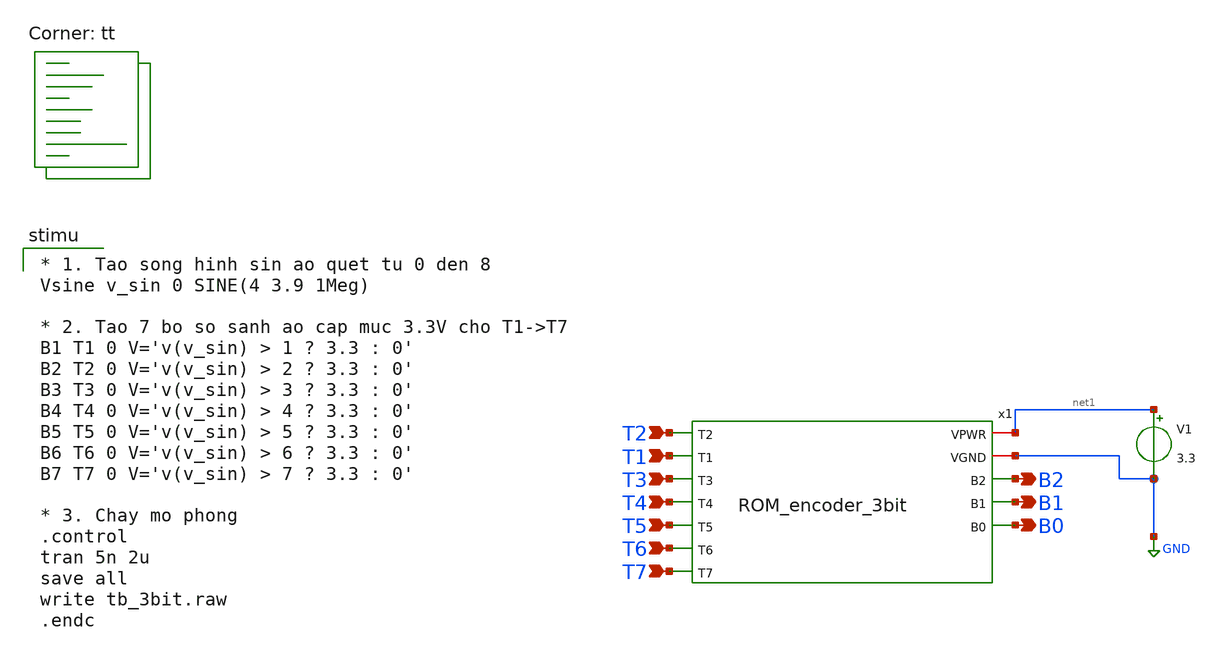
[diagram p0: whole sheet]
** sch_path: tb_rom_encoder_3bit.sch
**.subckt tb_rom_encoder_3bit T1 T2 T3 T4 T5 T6 T7 B2 B1 B0
*.ipin T1
*.ipin T2
*.ipin T3
*.ipin T4
*.ipin T5
*.ipin T6
*.ipin T7
*.opin B2
*.opin B1
*.opin B0
V1 net1 GND 3.3
x1 net1 T2 T1 T3 T4 T5 T6 T7 GND B2 B1 B0 ROM_encoder_3bit
**** begin user architecture code

* 1. Tao song hinh sin ao quet tu 0 den 8
Vsine v_sin 0 SINE(4 3.9 1Meg)

* 2. Tao 7 bo so sanh ao cap muc 3.3V cho T1->T7
B1 T1 0 V='v(v_sin) > 1 ? 3.3 : 0'
B2 T2 0 V='v(v_sin) > 2 ? 3.3 : 0'
B3 T3 0 V='v(v_sin) > 3 ? 3.3 : 0'
B4 T4 0 V='v(v_sin) > 4 ? 3.3 : 0'
B5 T5 0 V='v(v_sin) > 5 ? 3.3 : 0'
B6 T6 0 V='v(v_sin) > 6 ? 3.3 : 0'
B7 T7 0 V='v(v_sin) > 7 ? 3.3 : 0'

* 3. Chay mo phong
.control
tran 5n 2u
save all
write tb_3bit.raw
.endc

.lib $::SKYWATER_MODELS/sky130.lib.spice tt
**** end user architecture code
**.ends

* expanding   symbol:  /home/huydq/ROM_encoder_3bit.sym # of pins=12
** sym_path: ROM_encoder_3bit.sym
** sch_path: ROM_encoder_3bit.sch
.subckt ROM_encoder_3bit VPWR T2 T1 T3 T4 T5 T6 T7 VGND B2 B1 B0
*.ipin T1
*.ipin T2
*.ipin T3
*.ipin T4
*.ipin T5
*.ipin T6
*.ipin T7
*.iopin VGND
*.iopin VPWR
*.opin B0
*.opin B1
*.opin B2
x1 VPWR T2 T1 net4 VGND edge_cell
x2 VPWR T3 T2 net5 VGND edge_cell
x3 VPWR T4 T3 net6 VGND edge_cell
x4 VPWR T5 T4 net7 VGND edge_cell
x5 VPWR T6 T5 net8 VGND edge_cell
x6 VPWR T7 T6 net9 VGND edge_cell
x7 VPWR GND T7 net10 VGND edge_cell
XM7 net1 VGND VPWR VPWR sky130_fd_pr__pfet_g5v0d10v5 L=0.5 W=1 nf=1 ad='int((nf+1)/2) * W/nf * 0.29'
+ as='int((nf+2)/2) * W/nf * 0.29' pd='2*int((nf+1)/2) * (W/nf + 0.29)' ps='2*int((nf+2)/2) * (W/nf + 0.29)'
+ nrd='0.29 / W' nrs='0.29 / W' sa=0 sb=0 sd=0 mult=1 m=1
XM1 net2 VGND VPWR VPWR sky130_fd_pr__pfet_g5v0d10v5 L=0.5 W=1 nf=1 ad='int((nf+1)/2) * W/nf * 0.29'
+ as='int((nf+2)/2) * W/nf * 0.29' pd='2*int((nf+1)/2) * (W/nf + 0.29)' ps='2*int((nf+2)/2) * (W/nf + 0.29)'
+ nrd='0.29 / W' nrs='0.29 / W' sa=0 sb=0 sd=0 mult=1 m=1
XM2 net3 VGND VPWR VPWR sky130_fd_pr__pfet_g5v0d10v5 L=0.5 W=1 nf=1 ad='int((nf+1)/2) * W/nf * 0.29'
+ as='int((nf+2)/2) * W/nf * 0.29' pd='2*int((nf+1)/2) * (W/nf + 0.29)' ps='2*int((nf+2)/2) * (W/nf + 0.29)'
+ nrd='0.29 / W' nrs='0.29 / W' sa=0 sb=0 sd=0 mult=1 m=1
x8 VPWR net1 B0 VGND my_inv_1
x9 VPWR net2 B1 VGND my_inv_1
x10 VPWR net3 B2 VGND my_inv_1
XM3 net1 net4 GND GND sky130_fd_pr__nfet_g5v0d10v5 L=0.5 W=1 nf=1 ad='int((nf+1)/2) * W/nf * 0.29' as='int((nf+2)/2) * W/nf * 0.29'
+ pd='2*int((nf+1)/2) * (W/nf + 0.29)' ps='2*int((nf+2)/2) * (W/nf + 0.29)' nrd='0.29 / W' nrs='0.29 / W'
+ sa=0 sb=0 sd=0 mult=1 m=1
XM4 net2 net5 GND GND sky130_fd_pr__nfet_g5v0d10v5 L=0.5 W=1 nf=1 ad='int((nf+1)/2) * W/nf * 0.29' as='int((nf+2)/2) * W/nf * 0.29'
+ pd='2*int((nf+1)/2) * (W/nf + 0.29)' ps='2*int((nf+2)/2) * (W/nf + 0.29)' nrd='0.29 / W' nrs='0.29 / W'
+ sa=0 sb=0 sd=0 mult=1 m=1
XM5 net1 net6 GND GND sky130_fd_pr__nfet_g5v0d10v5 L=0.5 W=1 nf=1 ad='int((nf+1)/2) * W/nf * 0.29' as='int((nf+2)/2) * W/nf * 0.29'
+ pd='2*int((nf+1)/2) * (W/nf + 0.29)' ps='2*int((nf+2)/2) * (W/nf + 0.29)' nrd='0.29 / W' nrs='0.29 / W'
+ sa=0 sb=0 sd=0 mult=1 m=1
XM6 net2 net6 GND GND sky130_fd_pr__nfet_g5v0d10v5 L=0.5 W=1 nf=1 ad='int((nf+1)/2) * W/nf * 0.29' as='int((nf+2)/2) * W/nf * 0.29'
+ pd='2*int((nf+1)/2) * (W/nf + 0.29)' ps='2*int((nf+2)/2) * (W/nf + 0.29)' nrd='0.29 / W' nrs='0.29 / W'
+ sa=0 sb=0 sd=0 mult=1 m=1
XM8 net3 net7 GND GND sky130_fd_pr__nfet_g5v0d10v5 L=0.5 W=1 nf=1 ad='int((nf+1)/2) * W/nf * 0.29' as='int((nf+2)/2) * W/nf * 0.29'
+ pd='2*int((nf+1)/2) * (W/nf + 0.29)' ps='2*int((nf+2)/2) * (W/nf + 0.29)' nrd='0.29 / W' nrs='0.29 / W'
+ sa=0 sb=0 sd=0 mult=1 m=1
XM9 net1 net8 GND GND sky130_fd_pr__nfet_g5v0d10v5 L=0.5 W=1 nf=1 ad='int((nf+1)/2) * W/nf * 0.29' as='int((nf+2)/2) * W/nf * 0.29'
+ pd='2*int((nf+1)/2) * (W/nf + 0.29)' ps='2*int((nf+2)/2) * (W/nf + 0.29)' nrd='0.29 / W' nrs='0.29 / W'
+ sa=0 sb=0 sd=0 mult=1 m=1
XM10 net3 net8 GND GND sky130_fd_pr__nfet_g5v0d10v5 L=0.5 W=1 nf=1 ad='int((nf+1)/2) * W/nf * 0.29' as='int((nf+2)/2) * W/nf * 0.29'
+ pd='2*int((nf+1)/2) * (W/nf + 0.29)' ps='2*int((nf+2)/2) * (W/nf + 0.29)' nrd='0.29 / W' nrs='0.29 / W'
+ sa=0 sb=0 sd=0 mult=1 m=1
XM11 net2 net9 GND GND sky130_fd_pr__nfet_g5v0d10v5 L=0.5 W=1 nf=1 ad='int((nf+1)/2) * W/nf * 0.29' as='int((nf+2)/2) * W/nf * 0.29'
+ pd='2*int((nf+1)/2) * (W/nf + 0.29)' ps='2*int((nf+2)/2) * (W/nf + 0.29)' nrd='0.29 / W' nrs='0.29 / W'
+ sa=0 sb=0 sd=0 mult=1 m=1
XM12 net3 net9 GND GND sky130_fd_pr__nfet_g5v0d10v5 L=0.5 W=1 nf=1 ad='int((nf+1)/2) * W/nf * 0.29' as='int((nf+2)/2) * W/nf * 0.29'
+ pd='2*int((nf+1)/2) * (W/nf + 0.29)' ps='2*int((nf+2)/2) * (W/nf + 0.29)' nrd='0.29 / W' nrs='0.29 / W'
+ sa=0 sb=0 sd=0 mult=1 m=1
XM13 net1 net10 GND GND sky130_fd_pr__nfet_g5v0d10v5 L=0.5 W=1 nf=1 ad='int((nf+1)/2) * W/nf * 0.29'
+ as='int((nf+2)/2) * W/nf * 0.29' pd='2*int((nf+1)/2) * (W/nf + 0.29)' ps='2*int((nf+2)/2) * (W/nf + 0.29)'
+ nrd='0.29 / W' nrs='0.29 / W' sa=0 sb=0 sd=0 mult=1 m=1
XM14 net2 net10 GND GND sky130_fd_pr__nfet_g5v0d10v5 L=0.5 W=1 nf=1 ad='int((nf+1)/2) * W/nf * 0.29'
+ as='int((nf+2)/2) * W/nf * 0.29' pd='2*int((nf+1)/2) * (W/nf + 0.29)' ps='2*int((nf+2)/2) * (W/nf + 0.29)'
+ nrd='0.29 / W' nrs='0.29 / W' sa=0 sb=0 sd=0 mult=1 m=1
XM15 net3 net10 GND GND sky130_fd_pr__nfet_g5v0d10v5 L=0.5 W=1 nf=1 ad='int((nf+1)/2) * W/nf * 0.29'
+ as='int((nf+2)/2) * W/nf * 0.29' pd='2*int((nf+1)/2) * (W/nf + 0.29)' ps='2*int((nf+2)/2) * (W/nf + 0.29)'
+ nrd='0.29 / W' nrs='0.29 / W' sa=0 sb=0 sd=0 mult=1 m=1
.ends


* expanding   symbol:  /home/huydq/edge_cell.sym # of pins=5
** sym_path: edge_cell.sym
** sch_path: edge_cell.sch
.subckt edge_cell VPWR T_next T_in X_out VGND
*.ipin T_next
*.ipin T_in
*.opin X_out
*.iopin VPWR
*.iopin VGND
x1 VPWR T_next net2 VGND my_inv_1
x2 VPWR net1 X_out VGND my_inv_1
x3 VPWR net1 T_in net2 VGND my_nand_2
.ends


* expanding   symbol:  /home/huydq/my_inv_1.sym # of pins=4
** sym_path: my_inv_1.sym
** sch_path: my_inv_1.sch
.subckt my_inv_1 VPWR Vin Vout VGND
*.iopin VGND
*.iopin VPWR
*.ipin Vin
*.opin Vout
XM1 Vout Vin VGND VGND sky130_fd_pr__nfet_g5v0d10v5 L=0.5 W=1 nf=1 ad='int((nf+1)/2) * W/nf * 0.29' as='int((nf+2)/2) * W/nf * 0.29'
+ pd='2*int((nf+1)/2) * (W/nf + 0.29)' ps='2*int((nf+2)/2) * (W/nf + 0.29)' nrd='0.29 / W' nrs='0.29 / W'
+ sa=0 sb=0 sd=0 mult=1 m=1
XM2 Vout Vin VPWR VPWR sky130_fd_pr__pfet_g5v0d10v5 L=0.5 W=1 nf=1 ad='int((nf+1)/2) * W/nf * 0.29' as='int((nf+2)/2) * W/nf * 0.29'
+ pd='2*int((nf+1)/2) * (W/nf + 0.29)' ps='2*int((nf+2)/2) * (W/nf + 0.29)' nrd='0.29 / W' nrs='0.29 / W'
+ sa=0 sb=0 sd=0 mult=1 m=1
.ends


* expanding   symbol:  /home/huydq/my_nand_2.sym # of pins=5
** sym_path: my_nand_2.sym
** sch_path: my_nand_2.sch
.subckt my_nand_2 VPWR Y A B VGND
*.iopin VPWR
*.iopin VGND
*.ipin A
*.ipin B
*.opin Y
XM5 Y B net1 VGND sky130_fd_pr__nfet_g5v0d10v5 L=0.5 W=1 nf=1 ad='int((nf+1)/2) * W/nf * 0.29' as='int((nf+2)/2) * W/nf * 0.29'
+ pd='2*int((nf+1)/2) * (W/nf + 0.29)' ps='2*int((nf+2)/2) * (W/nf + 0.29)' nrd='0.29 / W' nrs='0.29 / W'
+ sa=0 sb=0 sd=0 mult=1 m=1
XM6 Y B VPWR VPWR sky130_fd_pr__pfet_g5v0d10v5 L=0.5 W=1 nf=1 ad='int((nf+1)/2) * W/nf * 0.29' as='int((nf+2)/2) * W/nf * 0.29'
+ pd='2*int((nf+1)/2) * (W/nf + 0.29)' ps='2*int((nf+2)/2) * (W/nf + 0.29)' nrd='0.29 / W' nrs='0.29 / W'
+ sa=0 sb=0 sd=0 mult=1 m=1
XM2 Y A VPWR VPWR sky130_fd_pr__pfet_g5v0d10v5 L=0.5 W=1 nf=1 ad='int((nf+1)/2) * W/nf * 0.29' as='int((nf+2)/2) * W/nf * 0.29'
+ pd='2*int((nf+1)/2) * (W/nf + 0.29)' ps='2*int((nf+2)/2) * (W/nf + 0.29)' nrd='0.29 / W' nrs='0.29 / W'
+ sa=0 sb=0 sd=0 mult=1 m=1
XM1 net1 A VGND VGND sky130_fd_pr__nfet_g5v0d10v5 L=0.5 W=1 nf=1 ad='int((nf+1)/2) * W/nf * 0.29' as='int((nf+2)/2) * W/nf * 0.29'
+ pd='2*int((nf+1)/2) * (W/nf + 0.29)' ps='2*int((nf+2)/2) * (W/nf + 0.29)' nrd='0.29 / W' nrs='0.29 / W'
+ sa=0 sb=0 sd=0 mult=1 m=1
.ends

.GLOBAL GND
.end
